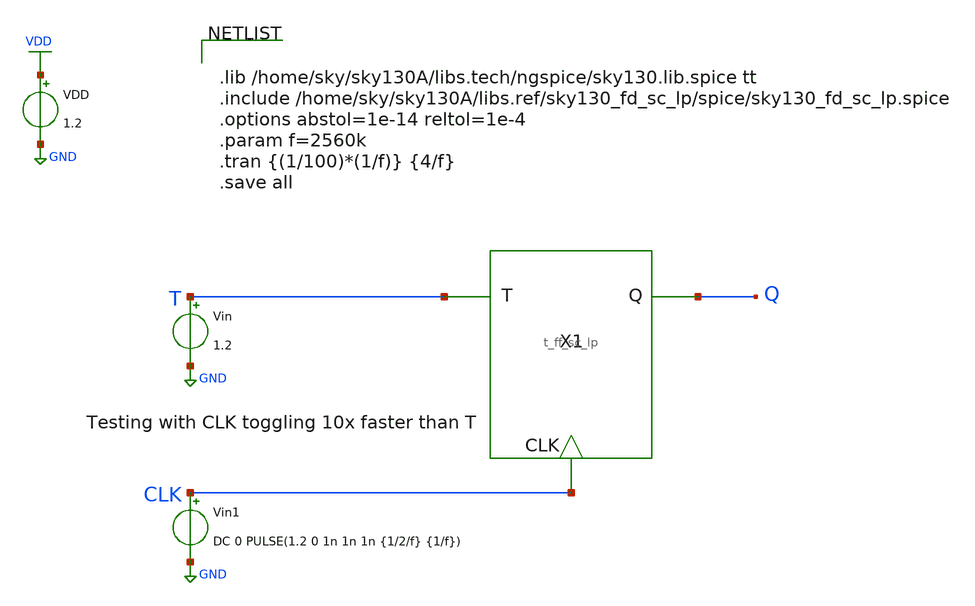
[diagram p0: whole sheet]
** sch_path: xschem/T_flip_flop/t_ff_sc_lp_tb.sch
**.subckt t_ff_sc_lp_tb
X1 T Q CLK t_ff_sc_lp
VDD VDD GND 1.2
Vin T GND 1.2
Vin1 CLK GND DC 0 PULSE(1.2 0 1n 1n 1n {1/2/f} {1/f})
**** begin user architecture code


.lib /home/sky/sky130A/libs.tech/ngspice/sky130.lib.spice tt
.include /home/sky/sky130A/libs.ref/sky130_fd_sc_lp/spice/sky130_fd_sc_lp.spice
.options abstol=1e-14 reltol=1e-4
.param f=2560k
.tran {(1/100)*(1/f)} {4/f}
.save all


**** end user architecture code
**.ends

* expanding   symbol:  T_flip_flop/t_ff_sc_lp.sym # of pins=3
** sym_path: xschem/T_flip_flop/t_ff_sc_lp.sym
** sch_path: xschem/T_flip_flop/t_ff_sc_lp.sch
.subckt t_ff_sc_lp T Q CLK
*.ipin T
*.ipin CLK
*.opin Q
x3 Q T GND GND VDD VDD net1 sky130_fd_sc_lp__xor2_1
x1 CLK net1 GND GND VDD VDD Q sky130_fd_sc_lp__dfxtp_1
.ends

.GLOBAL VDD
.GLOBAL GND
.end
